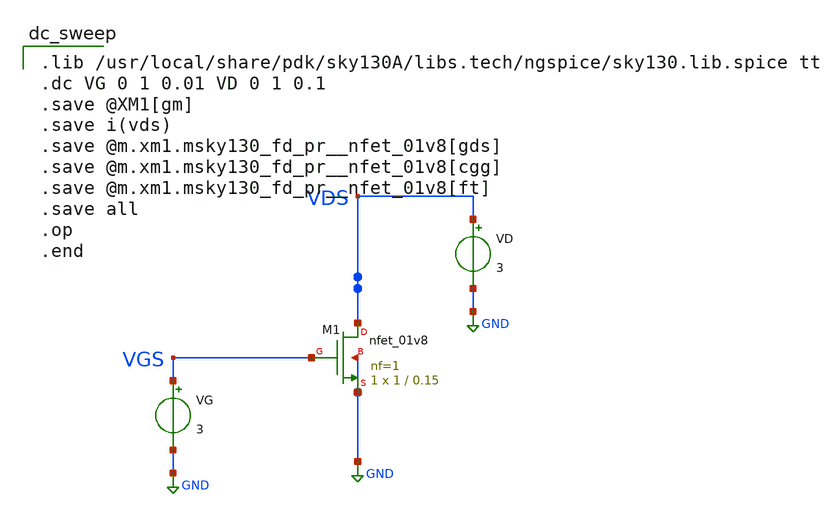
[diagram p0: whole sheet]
** sch_path: SKYWATER130_GMID/NMOS/DC_NFET1v8.sch
**.subckt DC_NFET1v8
XM1 VDS VGS GND GND sky130_fd_pr__nfet_01v8 L=0.15 W=1 nf=1 ad='int((nf+1)/2) * W/nf * 0.29' as='int((nf+2)/2) * W/nf * 0.29'
+ pd='2*int((nf+1)/2) * (W/nf + 0.29)' ps='2*int((nf+2)/2) * (W/nf + 0.29)' nrd='0.29 / W' nrs='0.29 / W'
+ sa=0 sb=0 sd=0 mult=1 m=1
VD VDS GND 3
VG VGS GND 3
**** begin user architecture code

.lib /usr/local/share/pdk/sky130A/libs.tech/ngspice/sky130.lib.spice tt
.dc VG 0 1 0.01 VD 0 1 0.1
.save @XM1[gm]
.save i(vds)
.save @m.xm1.msky130_fd_pr__nfet_01v8[gds]
.save @m.xm1.msky130_fd_pr__nfet_01v8[cgg]
.save @m.xm1.msky130_fd_pr__nfet_01v8[ft]
.save all
.op
.end

**** end user architecture code
**.ends
.GLOBAL GND
.end
